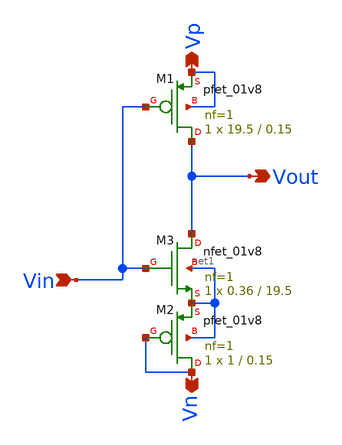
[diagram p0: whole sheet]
** sch_path: xschem/Vth_sch/Symbol/Inverter-th14.sch
**.subckt Inverter-th14 Vin Vout Vp Vn
*.ipin Vin
*.opin Vout
*.opin Vp
*.opin Vn
XM1 Vout Vin Vp Vp sky130_fd_pr__pfet_01v8 L=0.15 W=19.5 nf=1 ad='int((nf+1)/2) * W/nf * 0.29' as='int((nf+2)/2) * W/nf * 0.29'
+ pd='2*int((nf+1)/2) * (W/nf + 0.29)' ps='2*int((nf+2)/2) * (W/nf + 0.29)' nrd='0.29 / W' nrs='0.29 / W'
+ sa=0 sb=0 sd=0 mult=1 m=1
XM3 Vout Vin net1 net1 sky130_fd_pr__nfet_01v8 L=19.5 W=0.36 nf=1 ad='int((nf+1)/2) * W/nf * 0.29' as='int((nf+2)/2) * W/nf * 0.29'
+ pd='2*int((nf+1)/2) * (W/nf + 0.29)' ps='2*int((nf+2)/2) * (W/nf + 0.29)' nrd='0.29 / W' nrs='0.29 / W'
+ sa=0 sb=0 sd=0 mult=1 m=1
XM2 Vn Vn net1 net1 sky130_fd_pr__pfet_01v8 L=0.15 W=1 nf=1 ad='int((nf+1)/2) * W/nf * 0.29' as='int((nf+2)/2) * W/nf * 0.29'
+ pd='2*int((nf+1)/2) * (W/nf + 0.29)' ps='2*int((nf+2)/2) * (W/nf + 0.29)' nrd='0.29 / W' nrs='0.29 / W'
+ sa=0 sb=0 sd=0 mult=1 m=1
**.ends
.end
